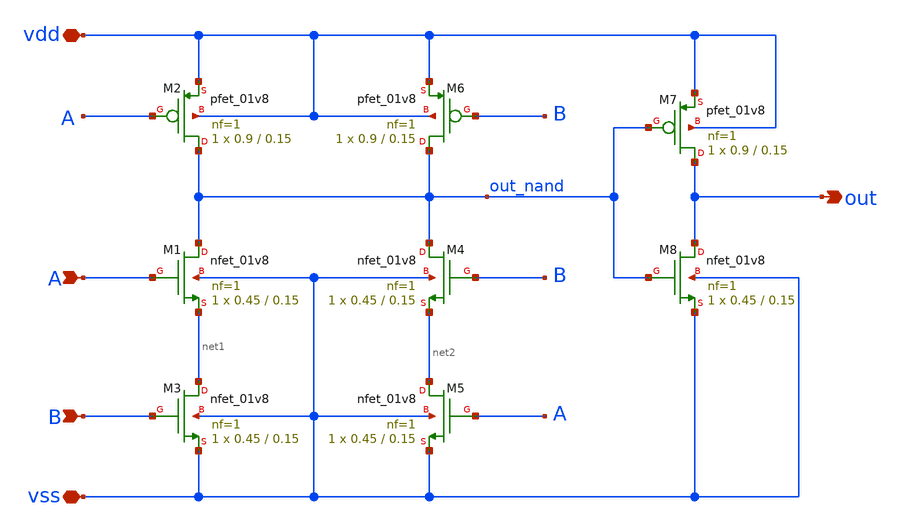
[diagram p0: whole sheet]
** sch_path: xschem/and_pfd.sch
**.subckt and_pfd vdd vss out A B
*.iopin vdd
*.iopin vss
*.opin out
*.ipin A
*.ipin B
XM1 out_nand A net1 vss sky130_fd_pr__nfet_01v8 L=0.15 W=0.45 nf=1 ad='int((nf+1)/2) * W/nf * 0.29' as='int((nf+2)/2) * W/nf * 0.29'
+ pd='2*int((nf+1)/2) * (W/nf + 0.29)' ps='2*int((nf+2)/2) * (W/nf + 0.29)' nrd='0.29 / W' nrs='0.29 / W'
+ sa=0 sb=0 sd=0 mult=1 m=1
XM2 out_nand A vdd vdd sky130_fd_pr__pfet_01v8 L=0.15 W=0.9 nf=1 ad='int((nf+1)/2) * W/nf * 0.29' as='int((nf+2)/2) * W/nf * 0.29'
+ pd='2*int((nf+1)/2) * (W/nf + 0.29)' ps='2*int((nf+2)/2) * (W/nf + 0.29)' nrd='0.29 / W' nrs='0.29 / W'
+ sa=0 sb=0 sd=0 mult=1 m=1
XM3 net1 B vss vss sky130_fd_pr__nfet_01v8 L=0.15 W=0.45 nf=1 ad='int((nf+1)/2) * W/nf * 0.29' as='int((nf+2)/2) * W/nf * 0.29'
+ pd='2*int((nf+1)/2) * (W/nf + 0.29)' ps='2*int((nf+2)/2) * (W/nf + 0.29)' nrd='0.29 / W' nrs='0.29 / W'
+ sa=0 sb=0 sd=0 mult=1 m=1
XM4 out_nand B net2 vss sky130_fd_pr__nfet_01v8 L=0.15 W=0.45 nf=1 ad='int((nf+1)/2) * W/nf * 0.29' as='int((nf+2)/2) * W/nf * 0.29'
+ pd='2*int((nf+1)/2) * (W/nf + 0.29)' ps='2*int((nf+2)/2) * (W/nf + 0.29)' nrd='0.29 / W' nrs='0.29 / W'
+ sa=0 sb=0 sd=0 mult=1 m=1
XM5 net2 A vss vss sky130_fd_pr__nfet_01v8 L=0.15 W=0.45 nf=1 ad='int((nf+1)/2) * W/nf * 0.29' as='int((nf+2)/2) * W/nf * 0.29'
+ pd='2*int((nf+1)/2) * (W/nf + 0.29)' ps='2*int((nf+2)/2) * (W/nf + 0.29)' nrd='0.29 / W' nrs='0.29 / W'
+ sa=0 sb=0 sd=0 mult=1 m=1
XM6 out_nand B vdd vdd sky130_fd_pr__pfet_01v8 L=0.15 W=0.9 nf=1 ad='int((nf+1)/2) * W/nf * 0.29' as='int((nf+2)/2) * W/nf * 0.29'
+ pd='2*int((nf+1)/2) * (W/nf + 0.29)' ps='2*int((nf+2)/2) * (W/nf + 0.29)' nrd='0.29 / W' nrs='0.29 / W'
+ sa=0 sb=0 sd=0 mult=1 m=1
XM7 out out_nand vdd vdd sky130_fd_pr__pfet_01v8 L=0.15 W=0.9 nf=1 ad='int((nf+1)/2) * W/nf * 0.29' as='int((nf+2)/2) * W/nf * 0.29'
+ pd='2*int((nf+1)/2) * (W/nf + 0.29)' ps='2*int((nf+2)/2) * (W/nf + 0.29)' nrd='0.29 / W' nrs='0.29 / W'
+ sa=0 sb=0 sd=0 mult=1 m=1
XM8 out out_nand vss vss sky130_fd_pr__nfet_01v8 L=0.15 W=0.45 nf=1 ad='int((nf+1)/2) * W/nf * 0.29'
+ as='int((nf+2)/2) * W/nf * 0.29' pd='2*int((nf+1)/2) * (W/nf + 0.29)' ps='2*int((nf+2)/2) * (W/nf + 0.29)'
+ nrd='0.29 / W' nrs='0.29 / W' sa=0 sb=0 sd=0 mult=1 m=1
**.ends
.end
